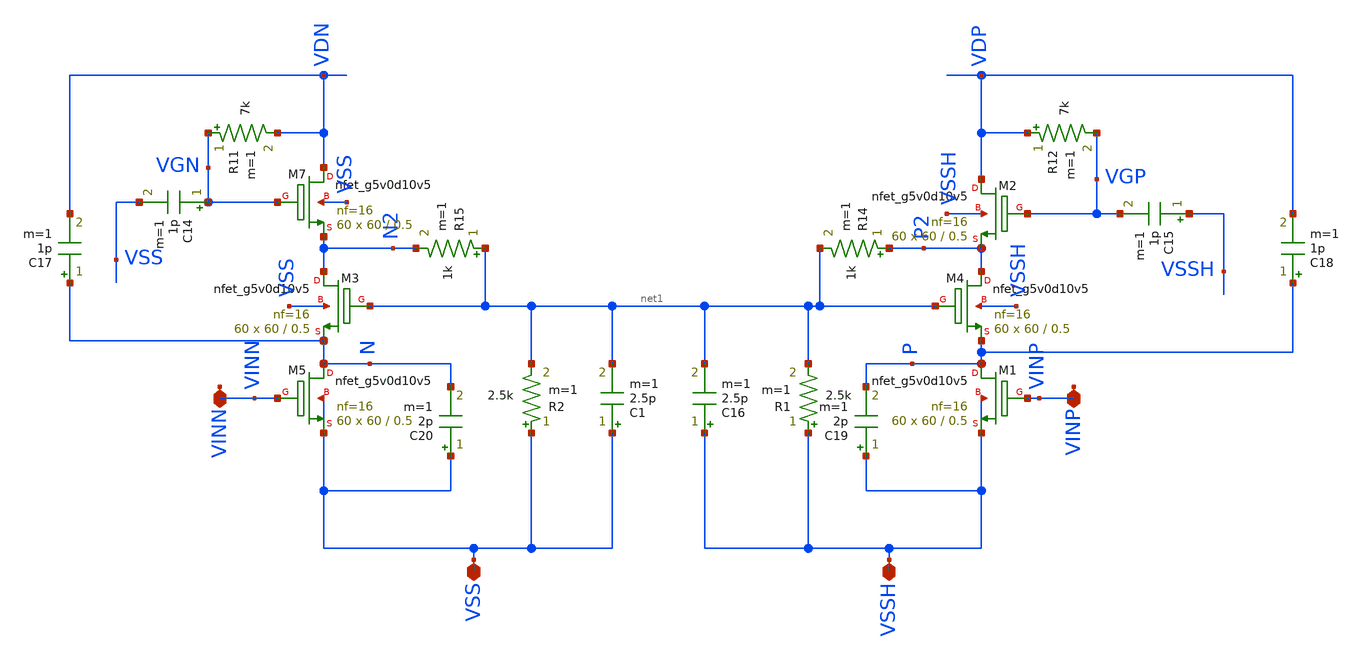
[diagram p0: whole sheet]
** sch_path: xschem/CLASSE_cascodes.sch
**.subckt CLASSE_cascodes VINP VSSH VINN VSS
*.iopin VINP
*.iopin VSSH
*.iopin VINN
*.iopin VSS
R12 VDP VGP 7k m=1
C15 VSSH VGP 1p m=1
R14 P2 net1 1k m=1
C18 P VDP 1p m=1
C19 VSSH P 2p m=1
R11 VGN VDN 7k m=1
C14 VGN VSS 1p m=1
R15 net1 N2 1k m=1
C17 N VDN 1p m=1
C20 VSS N 2p m=1
XM1 P VINP VSSH VSSH sky130_fd_pr__nfet_g5v0d10v5 L=0.5 W=60 nf=16 ad='int((nf+1)/2) * W/nf * 0.29' as='int((nf+2)/2) * W/nf * 0.29'
+ pd='2*int((nf+1)/2) * (W/nf + 0.29)' ps='2*int((nf+2)/2) * (W/nf + 0.29)' nrd='0.29 / W' nrs='0.29 / W'
+ sa=0 sb=0 sd=0 mult=60 m=60
XM2 VDP VGP P2 VSSH sky130_fd_pr__nfet_g5v0d10v5 L=0.5 W=60 nf=16 ad='int((nf+1)/2) * W/nf * 0.29' as='int((nf+2)/2) * W/nf * 0.29'
+ pd='2*int((nf+1)/2) * (W/nf + 0.29)' ps='2*int((nf+2)/2) * (W/nf + 0.29)' nrd='0.29 / W' nrs='0.29 / W'
+ sa=0 sb=0 sd=0 mult=60 m=60
XM3 N2 net1 N VSS sky130_fd_pr__nfet_g5v0d10v5 L=0.5 W=60 nf=16 ad='int((nf+1)/2) * W/nf * 0.29' as='int((nf+2)/2) * W/nf * 0.29'
+ pd='2*int((nf+1)/2) * (W/nf + 0.29)' ps='2*int((nf+2)/2) * (W/nf + 0.29)' nrd='0.29 / W' nrs='0.29 / W'
+ sa=0 sb=0 sd=0 mult=60 m=60
XM7 VDN VGN N2 VSS sky130_fd_pr__nfet_g5v0d10v5 L=0.5 W=60 nf=16 ad='int((nf+1)/2) * W/nf * 0.29' as='int((nf+2)/2) * W/nf * 0.29'
+ pd='2*int((nf+1)/2) * (W/nf + 0.29)' ps='2*int((nf+2)/2) * (W/nf + 0.29)' nrd='0.29 / W' nrs='0.29 / W'
+ sa=0 sb=0 sd=0 mult=60 m=60
XM4 P2 net1 P VSSH sky130_fd_pr__nfet_g5v0d10v5 L=0.5 W=60 nf=16 ad='int((nf+1)/2) * W/nf * 0.29' as='int((nf+2)/2) * W/nf * 0.29'
+ pd='2*int((nf+1)/2) * (W/nf + 0.29)' ps='2*int((nf+2)/2) * (W/nf + 0.29)' nrd='0.29 / W' nrs='0.29 / W'
+ sa=0 sb=0 sd=0 mult=60 m=60
XM5 N VINN VSS VSS sky130_fd_pr__nfet_g5v0d10v5 L=0.5 W=60 nf=16 ad='int((nf+1)/2) * W/nf * 0.29' as='int((nf+2)/2) * W/nf * 0.29'
+ pd='2*int((nf+1)/2) * (W/nf + 0.29)' ps='2*int((nf+2)/2) * (W/nf + 0.29)' nrd='0.29 / W' nrs='0.29 / W'
+ sa=0 sb=0 sd=0 mult=60 m=60
C16 VSSH net1 2.5p m=1
R1 VSSH net1 2.5k m=1
C1 VSS net1 2.5p m=1
R2 VSS net1 2.5k m=1
**.ends
.end
